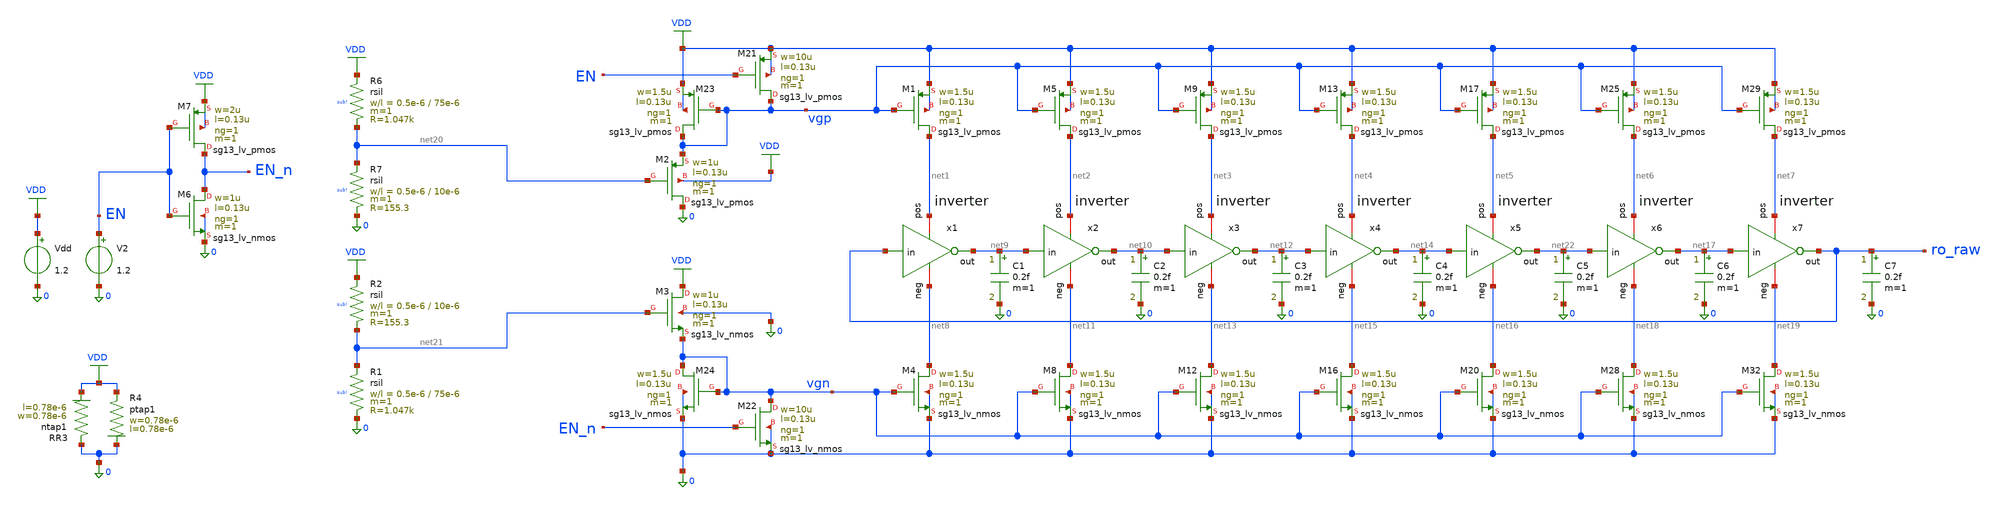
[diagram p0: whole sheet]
** sch_path: analog/temp-sens-core/temp-sens-core.sch
**.subckt temp-sens-core
XM1 net1 vgp VDD VDD sg13_lv_pmos w=1.5u l=0.13u ng=1 m=1 mm_ok=1
XM21 vgp EN VDD VDD sg13_lv_pmos w=10u l=0.13u ng=1 m=1 mm_ok=1
XM22 vgn EN_n 0 0 sg13_lv_nmos w=10u l=0.13u ng=1 m=1 mm_ok=1
XM23 vgp vgp VDD VDD sg13_lv_pmos w=1.5u l=0.13u ng=1 m=1 mm_ok=1
XM24 vgn vgn 0 0 sg13_lv_nmos w=1.5u l=0.13u ng=1 m=1 mm_ok=1
Vdd VDD 0 1.2
XR3 0 VDD ntap1 R=262.8 w=0.78e-6 l=0.78e-6
XR4 VDD 0 ptap1 R=262.8 w=0.78e-6 l=0.78e-6
XM4 net8 vgn 0 0 sg13_lv_nmos w=1.5u l=0.13u ng=1 m=1 mm_ok=1
XM5 net2 vgp VDD VDD sg13_lv_pmos w=1.5u l=0.13u ng=1 m=1 mm_ok=1
XM8 net11 vgn 0 0 sg13_lv_nmos w=1.5u l=0.13u ng=1 m=1 mm_ok=1
XM9 net3 vgp VDD VDD sg13_lv_pmos w=1.5u l=0.13u ng=1 m=1 mm_ok=1
XM12 net13 vgn 0 0 sg13_lv_nmos w=1.5u l=0.13u ng=1 m=1 mm_ok=1
XM13 net4 vgp VDD VDD sg13_lv_pmos w=1.5u l=0.13u ng=1 m=1 mm_ok=1
XM16 net15 vgn 0 0 sg13_lv_nmos w=1.5u l=0.13u ng=1 m=1 mm_ok=1
XM17 net5 vgp VDD VDD sg13_lv_pmos w=1.5u l=0.13u ng=1 m=1 mm_ok=1
XM20 net16 vgn 0 0 sg13_lv_nmos w=1.5u l=0.13u ng=1 m=1 mm_ok=1
XM25 net6 vgp VDD VDD sg13_lv_pmos w=1.5u l=0.13u ng=1 m=1 mm_ok=1
XM28 net18 vgn 0 0 sg13_lv_nmos w=1.5u l=0.13u ng=1 m=1 mm_ok=1
XM29 net7 vgp VDD VDD sg13_lv_pmos w=1.5u l=0.13u ng=1 m=1 mm_ok=1
XM32 net19 vgn 0 0 sg13_lv_nmos w=1.5u l=0.13u ng=1 m=1 mm_ok=1
x1 net1 ro_raw net9 net8 inverter
x2 net2 net9 net10 net11 inverter
x3 net3 net10 net12 net13 inverter
x4 net4 net12 net14 net15 inverter
x5 net5 net14 net22 net16 inverter
x6 net6 net22 net17 net18 inverter
x7 net7 net17 ro_raw net19 inverter
XM2 0 net20 vgp VDD sg13_lv_pmos w=1u l=0.13u ng=1 m=1 mm_ok=1
XM3 VDD net21 vgn 0 sg13_lv_nmos w=1u l=0.13u ng=1 m=1 mm_ok=1
XR6 VDD net20 sub! rsil w=0.5e-6 l=75e-6 m=1 mm_ok=1
XR7 net20 0 sub! rsil w=0.5e-6 l=10e-6 m=1 mm_ok=1
XR1 net21 0 sub! rsil w=0.5e-6 l=75e-6 m=1 mm_ok=1
XR2 VDD net21 sub! rsil w=0.5e-6 l=10e-6 m=1 mm_ok=1
C1 net9 0 0.2f m=1
C2 net10 0 0.2f m=1
C3 net12 0 0.2f m=1
C4 net14 0 0.2f m=1
C5 net22 0 0.2f m=1
C6 net17 0 0.2f m=1
C7 ro_raw 0 0.2f m=1
XM6 EN_n EN 0 0 sg13_lv_nmos w=1u l=0.13u ng=1 m=1 mm_ok=1
XM7 EN_n EN VDD VDD sg13_lv_pmos w=2u l=0.13u ng=1 m=1 mm_ok=1
V2 EN 0 1.2
**** begin user architecture code



* ngspice commands
.option rshunt=1e12
.option klu
.control

let temp_start = -25
let temp_stop = 145
let temp_delta = 5
compose temperature start=$&temp_start stop=$&temp_stop step=$&temp_delta
let frequency = vector(length(temperature))

let i = 0
let temp = temp_start
while temp le temp_stop
  option temp=$&temp

  tran 0.05n 100n
  meas tran tperiod
  + TRIG ro_raw VAL=0.6 RISE=2 TD=50n
  + TARG ro_raw VAL=0.6 RISE=3 TD=50n

  let frequency[i] = 1/tperiod

  let temp = temp + temp_delta
  let i = i+1
  if temp eq 25
    set medplot = $curplot
    let f = 1/tperiod
  end
end
let ro_raw = {$medplot}.ro_raw
let f = {$medplot}.f

settype frequency frequency
settype temperature temperature

write temp-sens-core.raw temperature frequency time ro_raw
.endc






.lib cornerMOSlv.lib mos_tt
.lib cornerMOShv.lib mos_tt
.lib cornerRES.lib res_typ
.lib cornerDIO.lib dio_tt






.include /foss/pdks/ihp-sg13cmos5l/libs.ref/sg13cmos5l_stdcell/spice/sg13cmos5l_stdcell.spice



**** end user architecture code
**.ends

* expanding   symbol:  analog/inverter/inverter.sym # of pins=4
** sym_path: analog/inverter/inverter.sym
** sch_path: analog/inverter/inverter.sch
.subckt inverter pos in out neg
*.ipin in
*.iopin pos
*.iopin neg
*.opin out
XM1 out in neg neg sg13_lv_nmos w=2.0u l=0.45u ng=1 m=1 mm_ok=1
XM2 pos in out pos sg13_lv_pmos w=1.0u l=0.45u ng=1 m=1 mm_ok=1
.ends

.GLOBAL VDD
.end
